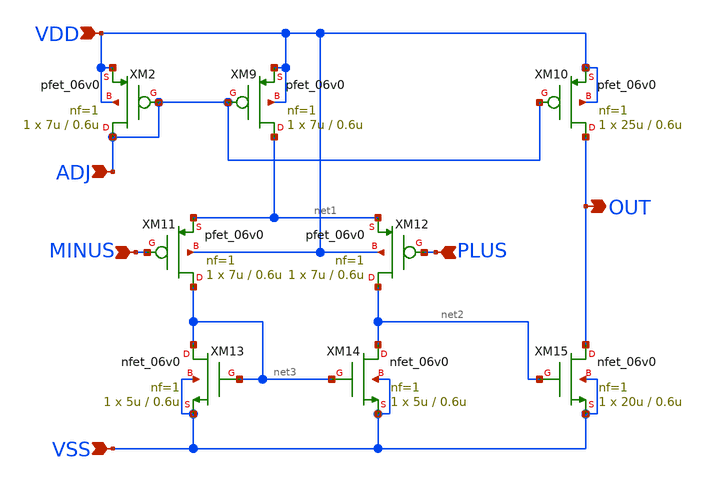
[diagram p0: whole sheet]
** sch_path: macros/Analog/R2R_DAC/xschem/opamp_slim.sch
**.subckt opamp_slim VDD PLUS VSS OUT MINUS ADJ
*.ipin VDD
*.ipin PLUS
*.ipin VSS
*.opin OUT
*.ipin MINUS
*.ipin ADJ
XM2 ADJ ADJ VDD VDD pfet_06v0 L=0.6u W=7u nf=1 ad='int((nf+1)/2) * W/nf * 0.18u' as='int((nf+2)/2) * W/nf * 0.18u'
+ pd='2*int((nf+1)/2) * (W/nf + 0.18u)' ps='2*int((nf+2)/2) * (W/nf + 0.18u)' nrd='0.18u / W' nrs='0.18u / W'
+ sa=0 sb=0 sd=0 m=1
XM9 net1 ADJ VDD VDD pfet_06v0 L=0.6u W=7u nf=1 ad='int((nf+1)/2) * W/nf * 0.18u' as='int((nf+2)/2) * W/nf * 0.18u'
+ pd='2*int((nf+1)/2) * (W/nf + 0.18u)' ps='2*int((nf+2)/2) * (W/nf + 0.18u)' nrd='0.18u / W' nrs='0.18u / W'
+ sa=0 sb=0 sd=0 m=1
XM10 OUT ADJ VDD VDD pfet_06v0 L=0.6u W=25u nf=1 ad='int((nf+1)/2) * W/nf * 0.18u' as='int((nf+2)/2) * W/nf * 0.18u'
+ pd='2*int((nf+1)/2) * (W/nf + 0.18u)' ps='2*int((nf+2)/2) * (W/nf + 0.18u)' nrd='0.18u / W' nrs='0.18u / W'
+ sa=0 sb=0 sd=0 m=1
XM11 net3 MINUS net1 VDD pfet_06v0 L=0.6u W=7u nf=1 ad='int((nf+1)/2) * W/nf * 0.18u' as='int((nf+2)/2) * W/nf * 0.18u'
+ pd='2*int((nf+1)/2) * (W/nf + 0.18u)' ps='2*int((nf+2)/2) * (W/nf + 0.18u)' nrd='0.18u / W' nrs='0.18u / W'
+ sa=0 sb=0 sd=0 m=1
XM12 net2 PLUS net1 VDD pfet_06v0 L=0.6u W=7u nf=1 ad='int((nf+1)/2) * W/nf * 0.18u' as='int((nf+2)/2) * W/nf * 0.18u'
+ pd='2*int((nf+1)/2) * (W/nf + 0.18u)' ps='2*int((nf+2)/2) * (W/nf + 0.18u)' nrd='0.18u / W' nrs='0.18u / W'
+ sa=0 sb=0 sd=0 m=1
XM13 net3 net3 VSS VSS nfet_06v0 L=0.6u W=5u nf=1 ad='int((nf+1)/2) * W/nf * 0.18u' as='int((nf+2)/2) * W/nf * 0.18u'
+ pd='2*int((nf+1)/2) * (W/nf + 0.18u)' ps='2*int((nf+2)/2) * (W/nf + 0.18u)' nrd='0.18u / W' nrs='0.18u / W'
+ sa=0 sb=0 sd=0 m=1
XM14 net2 net3 VSS VSS nfet_06v0 L=0.6u W=5u nf=1 ad='int((nf+1)/2) * W/nf * 0.18u' as='int((nf+2)/2) * W/nf * 0.18u'
+ pd='2*int((nf+1)/2) * (W/nf + 0.18u)' ps='2*int((nf+2)/2) * (W/nf + 0.18u)' nrd='0.18u / W' nrs='0.18u / W'
+ sa=0 sb=0 sd=0 m=1
XM15 OUT net2 VSS VSS nfet_06v0 L=0.6u W=20u nf=1 ad='int((nf+1)/2) * W/nf * 0.18u' as='int((nf+2)/2) * W/nf * 0.18u'
+ pd='2*int((nf+1)/2) * (W/nf + 0.18u)' ps='2*int((nf+2)/2) * (W/nf + 0.18u)' nrd='0.18u / W' nrs='0.18u / W'
+ sa=0 sb=0 sd=0 m=1
**.ends
.end
